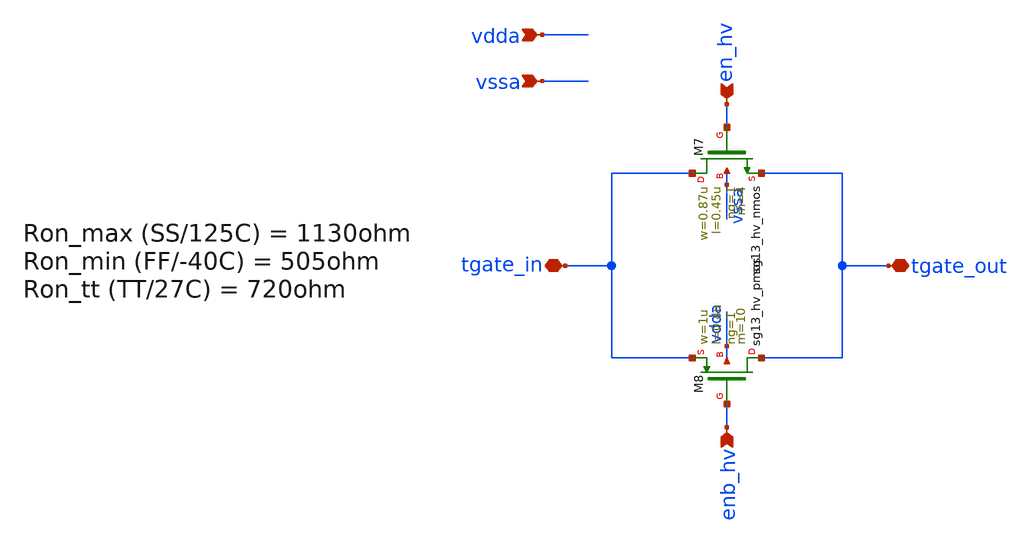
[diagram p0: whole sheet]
** sch_path: Schematics_Layout/sunrise_tgate_small/sunrise_tgate_small.sch
**.subckt sunrise_tgate_small vdda vssa tgate_in tgate_out en_hv enb_hv
*.ipin vdda
*.ipin vssa
*.iopin tgate_in
*.iopin tgate_out
*.ipin en_hv
*.ipin enb_hv
XM7 tgate_in en_hv tgate_out vssa sg13_hv_nmos w=0.87u l=0.45u ng=1 m=4 mm_ok=1
XM8 tgate_out enb_hv tgate_in vdda sg13_hv_pmos w=1u l=0.4u ng=1 m=10 mm_ok=1
**.ends
.end
